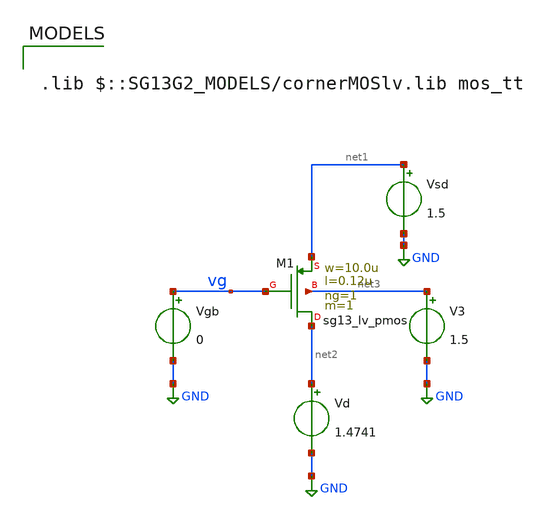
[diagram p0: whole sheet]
** sch_path: ihp_tutorials/Extraction/pmos_ext.sch
**.subckt pmos_ext
Vgb vg GND 0
Vsd net1 GND 1.5
V3 net3 GND 1.5
Vd net2 GND 1.4741
XM1 net2 vg net1 net3 sg13_lv_pmos w=10.0u l=0.12u ng=1 m=1 mm_ok=1
**** begin user architecture code



.control
pre_osdi ./psp103_nqs.osdi
save all
dc Vgb 0.05 1.5 1m

let gm_id = -deriv(ln(i(Vd)))
let id_gm = 1/gm_id
save gm_id id_gm

meas dc gm_id_max MAX gm_id
let gm_id_vt = 0.531*gm_id_max
save gm_id_vt

meas dc vt FIND V(vg) WHEN gm_id=gm_id_vt
let vt0=vt-1.5
meas dc is0_ FIND i(Vd) WHEN V(vg)=vt

let is0 = is0_/0.88
let VT_val=0.0259
let n = 1/(gm_id_max*VT_val)
save is0 vt0 n
echo
echo
echo

echo Extracted parameters:
print is0 vt0 n


echo
echo
echo

remzerovec
write pmos_ext.raw

.endc




.lib $::SG13G2_MODELS/cornerMOSlv.lib mos_tt

**** end user architecture code
**.ends
.GLOBAL GND
.end
